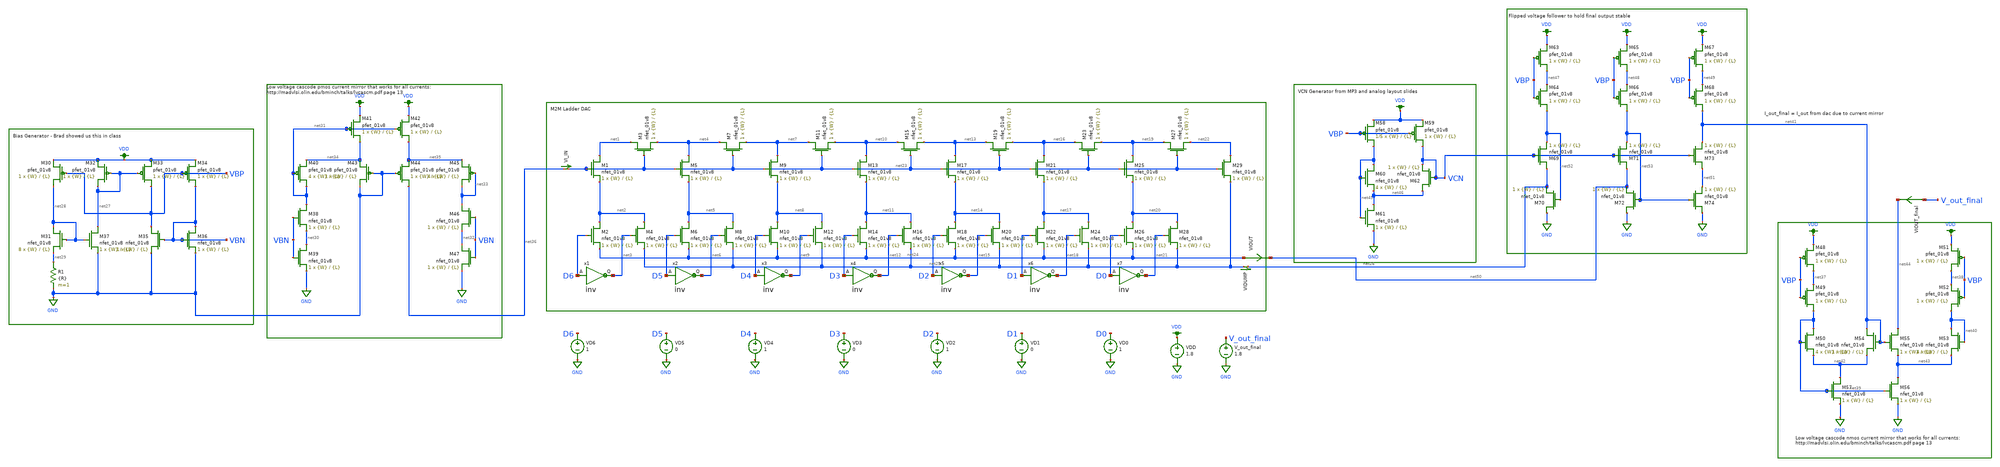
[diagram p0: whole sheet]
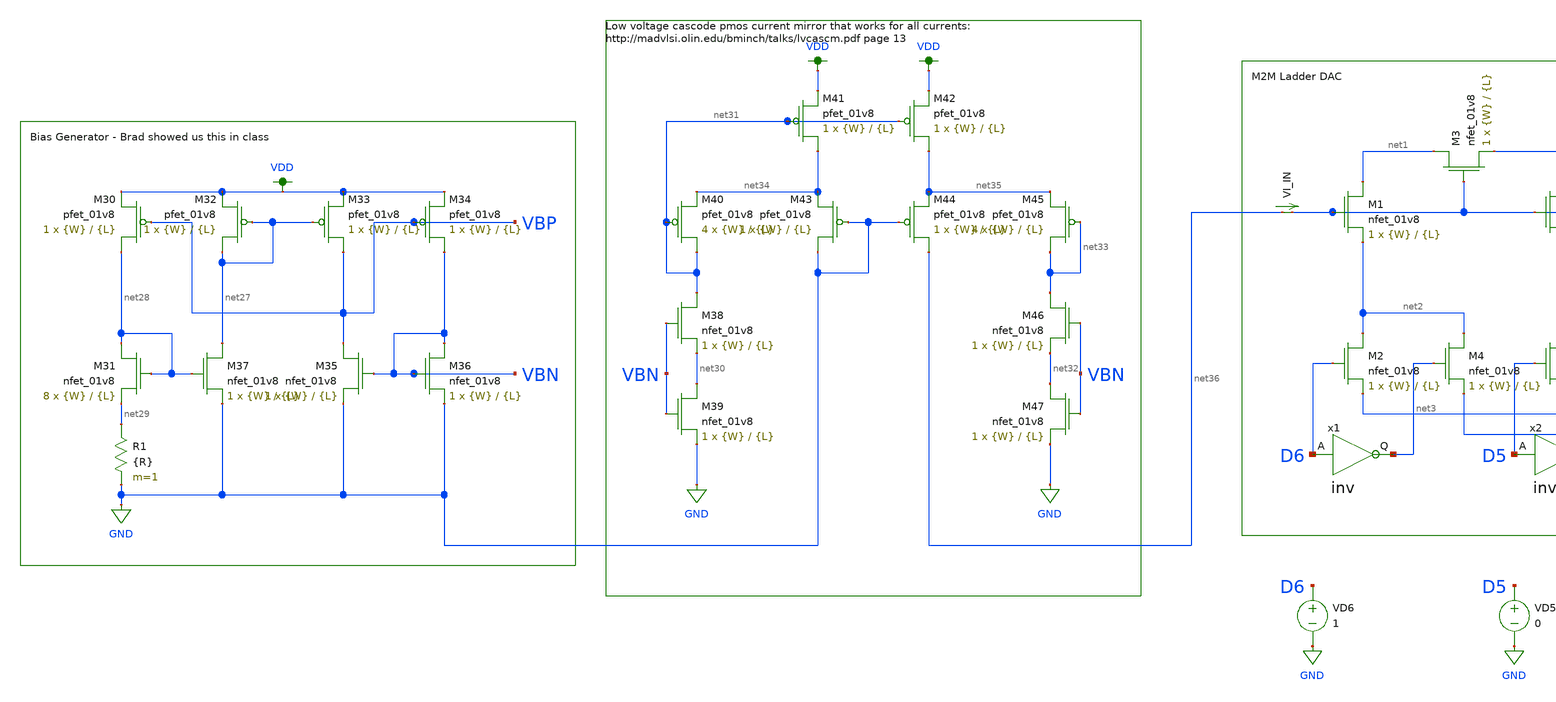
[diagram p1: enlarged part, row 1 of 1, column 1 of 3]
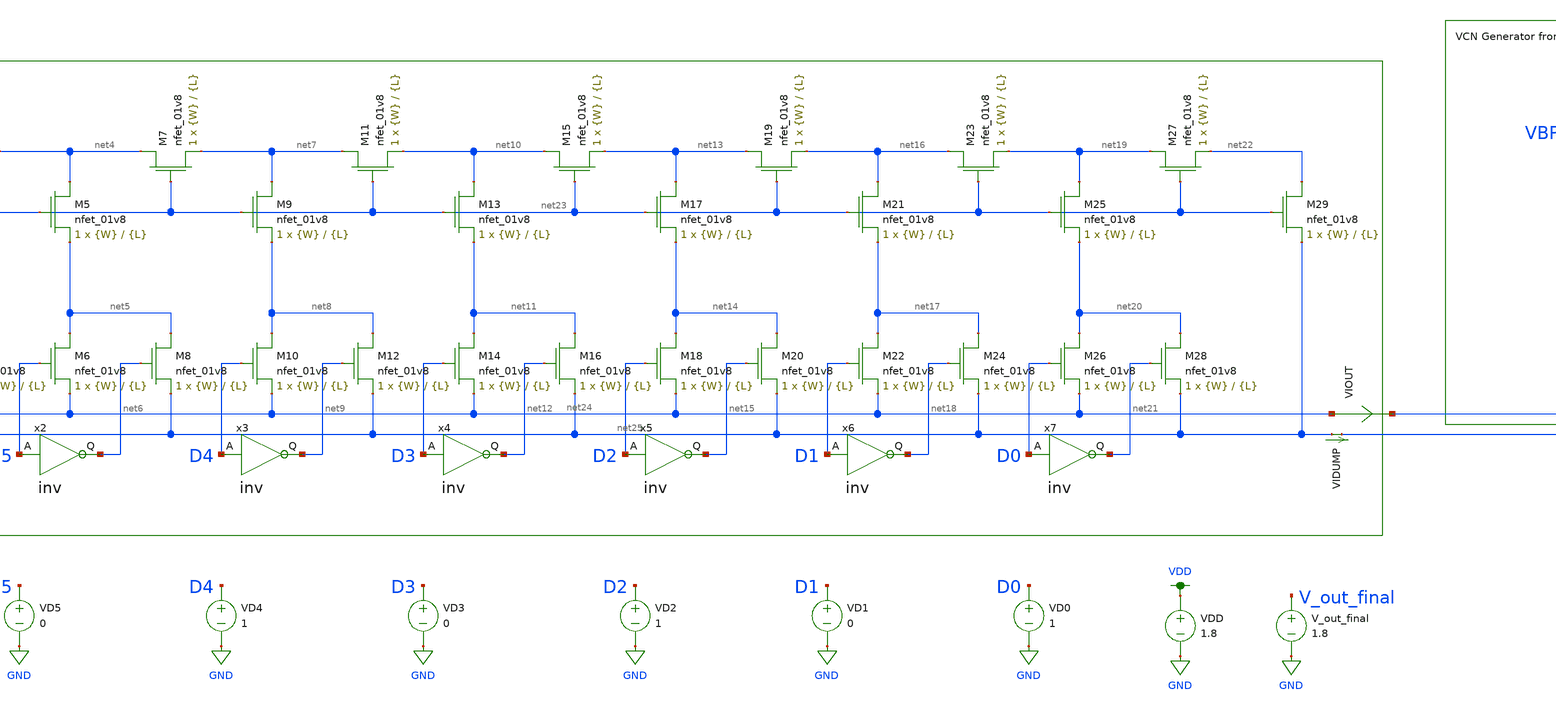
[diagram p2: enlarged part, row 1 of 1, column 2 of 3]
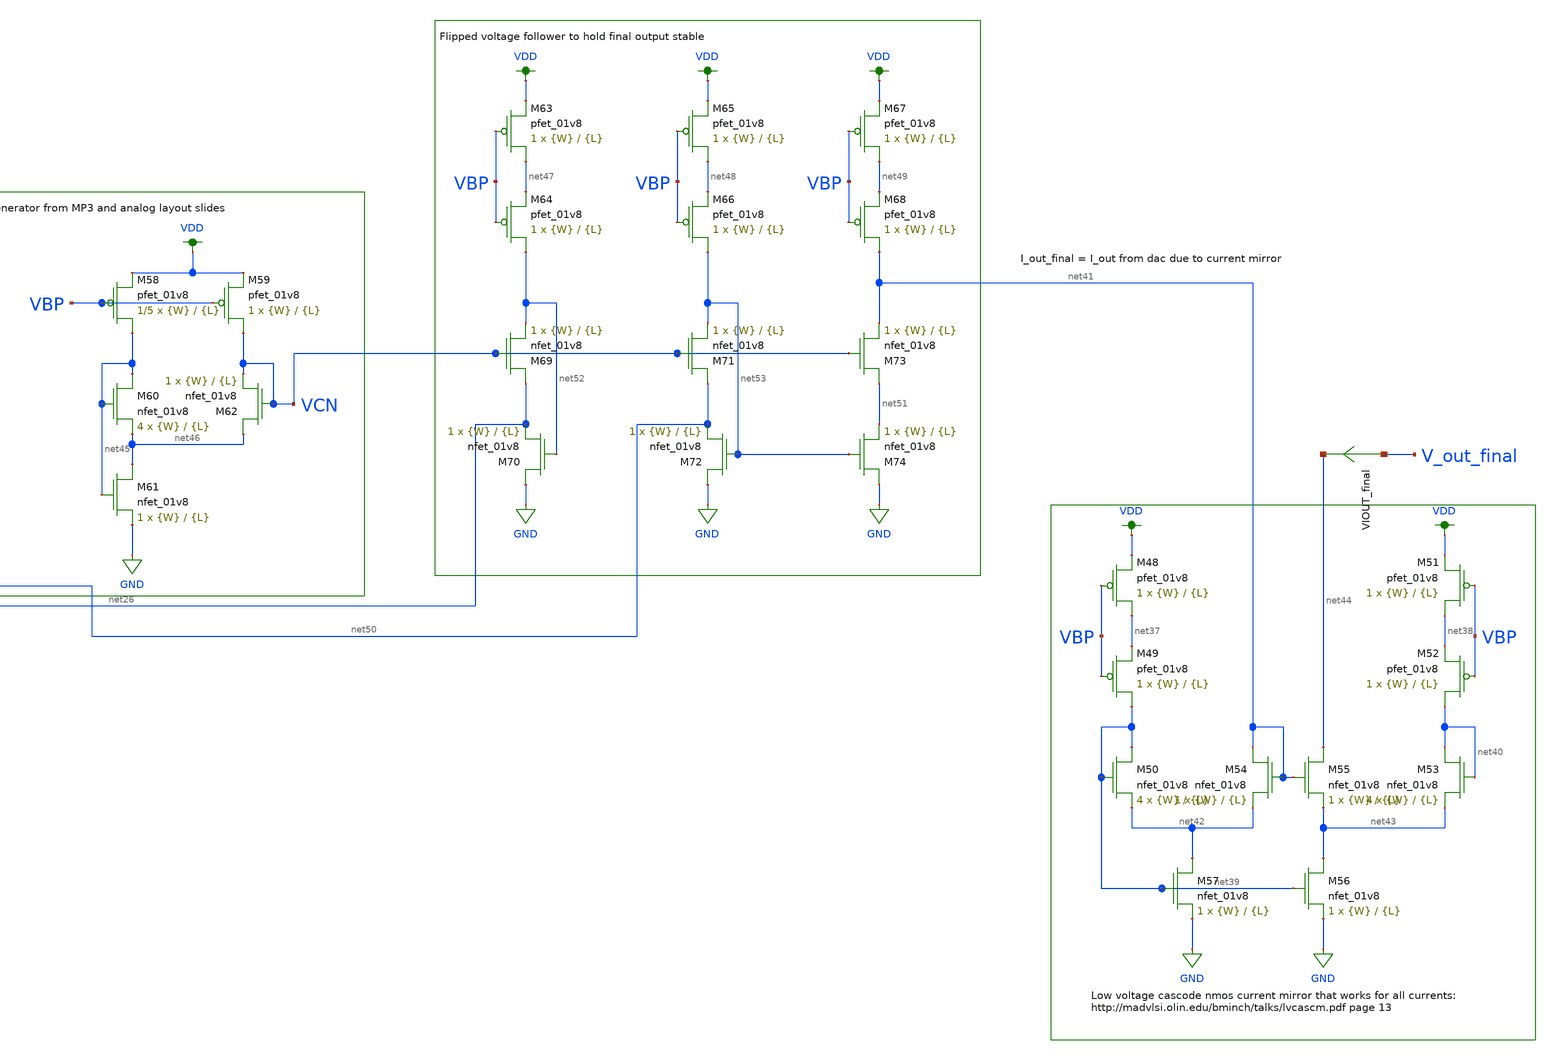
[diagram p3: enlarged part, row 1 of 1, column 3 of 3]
** sch_path: top_dac_VTC.sch
**.subckt top_dac_VTC
XM1 net1 net23 net2 GND sky130_fd_pr__nfet_01v8 L={L} W={W} nf=1 ad='int((nf+1)/2) * W/nf * 0.29' as='int((nf+2)/2) * W/nf * 0.29'
+ pd='2*int((nf+1)/2) * (W/nf + 0.29)' ps='2*int((nf+2)/2) * (W/nf + 0.29)' nrd='0.29 / W' nrs='0.29 / W'
+ sa=0 sb=0 sd=0 mult=1 m=1
XM2 net2 D6 net24 GND sky130_fd_pr__nfet_01v8 L={L} W={W} nf=1 ad='int((nf+1)/2) * W/nf * 0.29' as='int((nf+2)/2) * W/nf * 0.29'
+ pd='2*int((nf+1)/2) * (W/nf + 0.29)' ps='2*int((nf+2)/2) * (W/nf + 0.29)' nrd='0.29 / W' nrs='0.29 / W'
+ sa=0 sb=0 sd=0 mult=1 m=1
XM3 net1 net23 net4 GND sky130_fd_pr__nfet_01v8 L={L} W={W} nf=1 ad='int((nf+1)/2) * W/nf * 0.29' as='int((nf+2)/2) * W/nf * 0.29'
+ pd='2*int((nf+1)/2) * (W/nf + 0.29)' ps='2*int((nf+2)/2) * (W/nf + 0.29)' nrd='0.29 / W' nrs='0.29 / W'
+ sa=0 sb=0 sd=0 mult=1 m=1
XM4 net2 net3 net25 GND sky130_fd_pr__nfet_01v8 L={L} W={W} nf=1 ad='int((nf+1)/2) * W/nf * 0.29' as='int((nf+2)/2) * W/nf * 0.29'
+ pd='2*int((nf+1)/2) * (W/nf + 0.29)' ps='2*int((nf+2)/2) * (W/nf + 0.29)' nrd='0.29 / W' nrs='0.29 / W'
+ sa=0 sb=0 sd=0 mult=1 m=1
XM5 net4 net23 net5 GND sky130_fd_pr__nfet_01v8 L={L} W={W} nf=1 ad='int((nf+1)/2) * W/nf * 0.29' as='int((nf+2)/2) * W/nf * 0.29'
+ pd='2*int((nf+1)/2) * (W/nf + 0.29)' ps='2*int((nf+2)/2) * (W/nf + 0.29)' nrd='0.29 / W' nrs='0.29 / W'
+ sa=0 sb=0 sd=0 mult=1 m=1
XM6 net5 D5 net24 GND sky130_fd_pr__nfet_01v8 L={L} W={W} nf=1 ad='int((nf+1)/2) * W/nf * 0.29' as='int((nf+2)/2) * W/nf * 0.29'
+ pd='2*int((nf+1)/2) * (W/nf + 0.29)' ps='2*int((nf+2)/2) * (W/nf + 0.29)' nrd='0.29 / W' nrs='0.29 / W'
+ sa=0 sb=0 sd=0 mult=1 m=1
XM7 net4 net23 net7 GND sky130_fd_pr__nfet_01v8 L={L} W={W} nf=1 ad='int((nf+1)/2) * W/nf * 0.29' as='int((nf+2)/2) * W/nf * 0.29'
+ pd='2*int((nf+1)/2) * (W/nf + 0.29)' ps='2*int((nf+2)/2) * (W/nf + 0.29)' nrd='0.29 / W' nrs='0.29 / W'
+ sa=0 sb=0 sd=0 mult=1 m=1
XM8 net5 net6 net25 GND sky130_fd_pr__nfet_01v8 L={L} W={W} nf=1 ad='int((nf+1)/2) * W/nf * 0.29' as='int((nf+2)/2) * W/nf * 0.29'
+ pd='2*int((nf+1)/2) * (W/nf + 0.29)' ps='2*int((nf+2)/2) * (W/nf + 0.29)' nrd='0.29 / W' nrs='0.29 / W'
+ sa=0 sb=0 sd=0 mult=1 m=1
XM9 net7 net23 net8 GND sky130_fd_pr__nfet_01v8 L={L} W={W} nf=1 ad='int((nf+1)/2) * W/nf * 0.29' as='int((nf+2)/2) * W/nf * 0.29'
+ pd='2*int((nf+1)/2) * (W/nf + 0.29)' ps='2*int((nf+2)/2) * (W/nf + 0.29)' nrd='0.29 / W' nrs='0.29 / W'
+ sa=0 sb=0 sd=0 mult=1 m=1
XM10 net8 D4 net24 GND sky130_fd_pr__nfet_01v8 L={L} W={W} nf=1 ad='int((nf+1)/2) * W/nf * 0.29' as='int((nf+2)/2) * W/nf * 0.29'
+ pd='2*int((nf+1)/2) * (W/nf + 0.29)' ps='2*int((nf+2)/2) * (W/nf + 0.29)' nrd='0.29 / W' nrs='0.29 / W'
+ sa=0 sb=0 sd=0 mult=1 m=1
XM11 net7 net23 net10 GND sky130_fd_pr__nfet_01v8 L={L} W={W} nf=1 ad='int((nf+1)/2) * W/nf * 0.29' as='int((nf+2)/2) * W/nf * 0.29'
+ pd='2*int((nf+1)/2) * (W/nf + 0.29)' ps='2*int((nf+2)/2) * (W/nf + 0.29)' nrd='0.29 / W' nrs='0.29 / W'
+ sa=0 sb=0 sd=0 mult=1 m=1
XM12 net8 net9 net25 GND sky130_fd_pr__nfet_01v8 L={L} W={W} nf=1 ad='int((nf+1)/2) * W/nf * 0.29' as='int((nf+2)/2) * W/nf * 0.29'
+ pd='2*int((nf+1)/2) * (W/nf + 0.29)' ps='2*int((nf+2)/2) * (W/nf + 0.29)' nrd='0.29 / W' nrs='0.29 / W'
+ sa=0 sb=0 sd=0 mult=1 m=1
XM13 net10 net23 net11 GND sky130_fd_pr__nfet_01v8 L={L} W={W} nf=1 ad='int((nf+1)/2) * W/nf * 0.29'
+ as='int((nf+2)/2) * W/nf * 0.29' pd='2*int((nf+1)/2) * (W/nf + 0.29)' ps='2*int((nf+2)/2) * (W/nf + 0.29)'
+ nrd='0.29 / W' nrs='0.29 / W' sa=0 sb=0 sd=0 mult=1 m=1
XM14 net11 D3 net24 GND sky130_fd_pr__nfet_01v8 L={L} W={W} nf=1 ad='int((nf+1)/2) * W/nf * 0.29' as='int((nf+2)/2) * W/nf * 0.29'
+ pd='2*int((nf+1)/2) * (W/nf + 0.29)' ps='2*int((nf+2)/2) * (W/nf + 0.29)' nrd='0.29 / W' nrs='0.29 / W'
+ sa=0 sb=0 sd=0 mult=1 m=1
XM15 net10 net23 net13 GND sky130_fd_pr__nfet_01v8 L={L} W={W} nf=1 ad='int((nf+1)/2) * W/nf * 0.29'
+ as='int((nf+2)/2) * W/nf * 0.29' pd='2*int((nf+1)/2) * (W/nf + 0.29)' ps='2*int((nf+2)/2) * (W/nf + 0.29)'
+ nrd='0.29 / W' nrs='0.29 / W' sa=0 sb=0 sd=0 mult=1 m=1
XM16 net11 net12 net25 GND sky130_fd_pr__nfet_01v8 L={L} W={W} nf=1 ad='int((nf+1)/2) * W/nf * 0.29'
+ as='int((nf+2)/2) * W/nf * 0.29' pd='2*int((nf+1)/2) * (W/nf + 0.29)' ps='2*int((nf+2)/2) * (W/nf + 0.29)'
+ nrd='0.29 / W' nrs='0.29 / W' sa=0 sb=0 sd=0 mult=1 m=1
XM17 net13 net23 net14 GND sky130_fd_pr__nfet_01v8 L={L} W={W} nf=1 ad='int((nf+1)/2) * W/nf * 0.29'
+ as='int((nf+2)/2) * W/nf * 0.29' pd='2*int((nf+1)/2) * (W/nf + 0.29)' ps='2*int((nf+2)/2) * (W/nf + 0.29)'
+ nrd='0.29 / W' nrs='0.29 / W' sa=0 sb=0 sd=0 mult=1 m=1
XM18 net14 D2 net24 GND sky130_fd_pr__nfet_01v8 L={L} W={W} nf=1 ad='int((nf+1)/2) * W/nf * 0.29' as='int((nf+2)/2) * W/nf * 0.29'
+ pd='2*int((nf+1)/2) * (W/nf + 0.29)' ps='2*int((nf+2)/2) * (W/nf + 0.29)' nrd='0.29 / W' nrs='0.29 / W'
+ sa=0 sb=0 sd=0 mult=1 m=1
XM19 net13 net23 net16 GND sky130_fd_pr__nfet_01v8 L={L} W={W} nf=1 ad='int((nf+1)/2) * W/nf * 0.29'
+ as='int((nf+2)/2) * W/nf * 0.29' pd='2*int((nf+1)/2) * (W/nf + 0.29)' ps='2*int((nf+2)/2) * (W/nf + 0.29)'
+ nrd='0.29 / W' nrs='0.29 / W' sa=0 sb=0 sd=0 mult=1 m=1
XM20 net14 net15 net25 GND sky130_fd_pr__nfet_01v8 L={L} W={W} nf=1 ad='int((nf+1)/2) * W/nf * 0.29'
+ as='int((nf+2)/2) * W/nf * 0.29' pd='2*int((nf+1)/2) * (W/nf + 0.29)' ps='2*int((nf+2)/2) * (W/nf + 0.29)'
+ nrd='0.29 / W' nrs='0.29 / W' sa=0 sb=0 sd=0 mult=1 m=1
XM21 net16 net23 net17 GND sky130_fd_pr__nfet_01v8 L={L} W={W} nf=1 ad='int((nf+1)/2) * W/nf * 0.29'
+ as='int((nf+2)/2) * W/nf * 0.29' pd='2*int((nf+1)/2) * (W/nf + 0.29)' ps='2*int((nf+2)/2) * (W/nf + 0.29)'
+ nrd='0.29 / W' nrs='0.29 / W' sa=0 sb=0 sd=0 mult=1 m=1
XM22 net17 D1 net24 GND sky130_fd_pr__nfet_01v8 L={L} W={W} nf=1 ad='int((nf+1)/2) * W/nf * 0.29' as='int((nf+2)/2) * W/nf * 0.29'
+ pd='2*int((nf+1)/2) * (W/nf + 0.29)' ps='2*int((nf+2)/2) * (W/nf + 0.29)' nrd='0.29 / W' nrs='0.29 / W'
+ sa=0 sb=0 sd=0 mult=1 m=1
XM23 net16 net23 net19 GND sky130_fd_pr__nfet_01v8 L={L} W={W} nf=1 ad='int((nf+1)/2) * W/nf * 0.29'
+ as='int((nf+2)/2) * W/nf * 0.29' pd='2*int((nf+1)/2) * (W/nf + 0.29)' ps='2*int((nf+2)/2) * (W/nf + 0.29)'
+ nrd='0.29 / W' nrs='0.29 / W' sa=0 sb=0 sd=0 mult=1 m=1
XM24 net17 net18 net25 GND sky130_fd_pr__nfet_01v8 L={L} W={W} nf=1 ad='int((nf+1)/2) * W/nf * 0.29'
+ as='int((nf+2)/2) * W/nf * 0.29' pd='2*int((nf+1)/2) * (W/nf + 0.29)' ps='2*int((nf+2)/2) * (W/nf + 0.29)'
+ nrd='0.29 / W' nrs='0.29 / W' sa=0 sb=0 sd=0 mult=1 m=1
XM25 net19 net23 net20 GND sky130_fd_pr__nfet_01v8 L={L} W={W} nf=1 ad='int((nf+1)/2) * W/nf * 0.29'
+ as='int((nf+2)/2) * W/nf * 0.29' pd='2*int((nf+1)/2) * (W/nf + 0.29)' ps='2*int((nf+2)/2) * (W/nf + 0.29)'
+ nrd='0.29 / W' nrs='0.29 / W' sa=0 sb=0 sd=0 mult=1 m=1
XM26 net20 D0 net24 GND sky130_fd_pr__nfet_01v8 L={L} W={W} nf=1 ad='int((nf+1)/2) * W/nf * 0.29' as='int((nf+2)/2) * W/nf * 0.29'
+ pd='2*int((nf+1)/2) * (W/nf + 0.29)' ps='2*int((nf+2)/2) * (W/nf + 0.29)' nrd='0.29 / W' nrs='0.29 / W'
+ sa=0 sb=0 sd=0 mult=1 m=1
XM27 net19 net23 net22 GND sky130_fd_pr__nfet_01v8 L={L} W={W} nf=1 ad='int((nf+1)/2) * W/nf * 0.29'
+ as='int((nf+2)/2) * W/nf * 0.29' pd='2*int((nf+1)/2) * (W/nf + 0.29)' ps='2*int((nf+2)/2) * (W/nf + 0.29)'
+ nrd='0.29 / W' nrs='0.29 / W' sa=0 sb=0 sd=0 mult=1 m=1
XM28 net20 net21 net25 GND sky130_fd_pr__nfet_01v8 L={L} W={W} nf=1 ad='int((nf+1)/2) * W/nf * 0.29'
+ as='int((nf+2)/2) * W/nf * 0.29' pd='2*int((nf+1)/2) * (W/nf + 0.29)' ps='2*int((nf+2)/2) * (W/nf + 0.29)'
+ nrd='0.29 / W' nrs='0.29 / W' sa=0 sb=0 sd=0 mult=1 m=1
XM29 net22 net23 net25 GND sky130_fd_pr__nfet_01v8 L={L} W={W} nf=1 ad='int((nf+1)/2) * W/nf * 0.29'
+ as='int((nf+2)/2) * W/nf * 0.29' pd='2*int((nf+1)/2) * (W/nf + 0.29)' ps='2*int((nf+2)/2) * (W/nf + 0.29)'
+ nrd='0.29 / W' nrs='0.29 / W' sa=0 sb=0 sd=0 mult=1 m=1
VIDUMP net25 net26 0
.save i(vidump)
VI_IN net36 net23 0
.save i(vi_in)
x1 net3 D6 inv
x2 net6 D5 inv
x3 net9 D4 inv
x4 net12 D3 inv
x5 net15 D2 inv
x6 net18 D1 inv
x7 net21 D0 inv
XM30 net28 VBP VDD VDD sky130_fd_pr__pfet_01v8 L={L} W={W} nf=1 ad='int((nf+1)/2) * W/nf * 0.29' as='int((nf+2)/2) * W/nf * 0.29'
+ pd='2*int((nf+1)/2) * (W/nf + 0.29)' ps='2*int((nf+2)/2) * (W/nf + 0.29)' nrd='0.29 / W' nrs='0.29 / W'
+ sa=0 sb=0 sd=0 mult=1 m=1
XM31 net28 net28 net29 GND sky130_fd_pr__nfet_01v8 L={L} W={W} nf=1 ad='int((nf+1)/2) * W/nf * 0.29'
+ as='int((nf+2)/2) * W/nf * 0.29' pd='2*int((nf+1)/2) * (W/nf + 0.29)' ps='2*int((nf+2)/2) * (W/nf + 0.29)'
+ nrd='0.29 / W' nrs='0.29 / W' sa=0 sb=0 sd=0 mult=8 m=8
XM32 net27 net27 VDD VDD sky130_fd_pr__pfet_01v8 L={L} W={W} nf=1 ad='int((nf+1)/2) * W/nf * 0.29' as='int((nf+2)/2) * W/nf * 0.29'
+ pd='2*int((nf+1)/2) * (W/nf + 0.29)' ps='2*int((nf+2)/2) * (W/nf + 0.29)' nrd='0.29 / W' nrs='0.29 / W'
+ sa=0 sb=0 sd=0 mult=1 m=1
XM33 VBP net27 VDD VDD sky130_fd_pr__pfet_01v8 L={L} W={W} nf=1 ad='int((nf+1)/2) * W/nf * 0.29' as='int((nf+2)/2) * W/nf * 0.29'
+ pd='2*int((nf+1)/2) * (W/nf + 0.29)' ps='2*int((nf+2)/2) * (W/nf + 0.29)' nrd='0.29 / W' nrs='0.29 / W'
+ sa=0 sb=0 sd=0 mult=1 m=1
XM34 VBN VBP VDD VDD sky130_fd_pr__pfet_01v8 L={L} W={W} nf=1 ad='int((nf+1)/2) * W/nf * 0.29' as='int((nf+2)/2) * W/nf * 0.29'
+ pd='2*int((nf+1)/2) * (W/nf + 0.29)' ps='2*int((nf+2)/2) * (W/nf + 0.29)' nrd='0.29 / W' nrs='0.29 / W'
+ sa=0 sb=0 sd=0 mult=1 m=1
XM35 VBP VBN GND GND sky130_fd_pr__nfet_01v8 L={L} W={W} nf=1 ad='int((nf+1)/2) * W/nf * 0.29' as='int((nf+2)/2) * W/nf * 0.29'
+ pd='2*int((nf+1)/2) * (W/nf + 0.29)' ps='2*int((nf+2)/2) * (W/nf + 0.29)' nrd='0.29 / W' nrs='0.29 / W'
+ sa=0 sb=0 sd=0 mult=1 m=1
XM36 VBN VBN GND GND sky130_fd_pr__nfet_01v8 L={L} W={W} nf=1 ad='int((nf+1)/2) * W/nf * 0.29' as='int((nf+2)/2) * W/nf * 0.29'
+ pd='2*int((nf+1)/2) * (W/nf + 0.29)' ps='2*int((nf+2)/2) * (W/nf + 0.29)' nrd='0.29 / W' nrs='0.29 / W'
+ sa=0 sb=0 sd=0 mult=1 m=1
XM37 net27 net28 GND GND sky130_fd_pr__nfet_01v8 L={L} W={W} nf=1 ad='int((nf+1)/2) * W/nf * 0.29' as='int((nf+2)/2) * W/nf * 0.29'
+ pd='2*int((nf+1)/2) * (W/nf + 0.29)' ps='2*int((nf+2)/2) * (W/nf + 0.29)' nrd='0.29 / W' nrs='0.29 / W'
+ sa=0 sb=0 sd=0 mult=1 m=1
R1 net29 GND {R} m=1
XM38 net31 VBN net30 GND sky130_fd_pr__nfet_01v8 L={L} W={W} nf=1 ad='int((nf+1)/2) * W/nf * 0.29' as='int((nf+2)/2) * W/nf * 0.29'
+ pd='2*int((nf+1)/2) * (W/nf + 0.29)' ps='2*int((nf+2)/2) * (W/nf + 0.29)' nrd='0.29 / W' nrs='0.29 / W'
+ sa=0 sb=0 sd=0 mult=1 m=1
XM39 net30 VBN GND GND sky130_fd_pr__nfet_01v8 L={L} W={W} nf=1 ad='int((nf+1)/2) * W/nf * 0.29' as='int((nf+2)/2) * W/nf * 0.29'
+ pd='2*int((nf+1)/2) * (W/nf + 0.29)' ps='2*int((nf+2)/2) * (W/nf + 0.29)' nrd='0.29 / W' nrs='0.29 / W'
+ sa=0 sb=0 sd=0 mult=1 m=1
XM40 net31 net31 net34 VDD sky130_fd_pr__pfet_01v8 L={L} W={W} nf=1 ad='int((nf+1)/2) * W/nf * 0.29'
+ as='int((nf+2)/2) * W/nf * 0.29' pd='2*int((nf+1)/2) * (W/nf + 0.29)' ps='2*int((nf+2)/2) * (W/nf + 0.29)'
+ nrd='0.29 / W' nrs='0.29 / W' sa=0 sb=0 sd=0 mult=4 m=4
XM41 net34 net31 VDD VDD sky130_fd_pr__pfet_01v8 L={L} W={W} nf=1 ad='int((nf+1)/2) * W/nf * 0.29' as='int((nf+2)/2) * W/nf * 0.29'
+ pd='2*int((nf+1)/2) * (W/nf + 0.29)' ps='2*int((nf+2)/2) * (W/nf + 0.29)' nrd='0.29 / W' nrs='0.29 / W'
+ sa=0 sb=0 sd=0 mult=1 m=1
XM42 net35 net31 VDD VDD sky130_fd_pr__pfet_01v8 L={L} W={W} nf=1 ad='int((nf+1)/2) * W/nf * 0.29' as='int((nf+2)/2) * W/nf * 0.29'
+ pd='2*int((nf+1)/2) * (W/nf + 0.29)' ps='2*int((nf+2)/2) * (W/nf + 0.29)' nrd='0.29 / W' nrs='0.29 / W'
+ sa=0 sb=0 sd=0 mult=1 m=1
XM43 GND GND net34 VDD sky130_fd_pr__pfet_01v8 L={L} W={W} nf=1 ad='int((nf+1)/2) * W/nf * 0.29' as='int((nf+2)/2) * W/nf * 0.29'
+ pd='2*int((nf+1)/2) * (W/nf + 0.29)' ps='2*int((nf+2)/2) * (W/nf + 0.29)' nrd='0.29 / W' nrs='0.29 / W'
+ sa=0 sb=0 sd=0 mult=1 m=1
XM44 net36 GND net35 VDD sky130_fd_pr__pfet_01v8 L={L} W={W} nf=1 ad='int((nf+1)/2) * W/nf * 0.29' as='int((nf+2)/2) * W/nf * 0.29'
+ pd='2*int((nf+1)/2) * (W/nf + 0.29)' ps='2*int((nf+2)/2) * (W/nf + 0.29)' nrd='0.29 / W' nrs='0.29 / W'
+ sa=0 sb=0 sd=0 mult=1 m=1
XM45 net33 net33 net35 VDD sky130_fd_pr__pfet_01v8 L={L} W={W} nf=1 ad='int((nf+1)/2) * W/nf * 0.29'
+ as='int((nf+2)/2) * W/nf * 0.29' pd='2*int((nf+1)/2) * (W/nf + 0.29)' ps='2*int((nf+2)/2) * (W/nf + 0.29)'
+ nrd='0.29 / W' nrs='0.29 / W' sa=0 sb=0 sd=0 mult=4 m=4
XM46 net33 VBN net32 GND sky130_fd_pr__nfet_01v8 L={L} W={W} nf=1 ad='int((nf+1)/2) * W/nf * 0.29' as='int((nf+2)/2) * W/nf * 0.29'
+ pd='2*int((nf+1)/2) * (W/nf + 0.29)' ps='2*int((nf+2)/2) * (W/nf + 0.29)' nrd='0.29 / W' nrs='0.29 / W'
+ sa=0 sb=0 sd=0 mult=1 m=1
XM47 net32 VBN GND GND sky130_fd_pr__nfet_01v8 L={L} W={W} nf=1 ad='int((nf+1)/2) * W/nf * 0.29' as='int((nf+2)/2) * W/nf * 0.29'
+ pd='2*int((nf+1)/2) * (W/nf + 0.29)' ps='2*int((nf+2)/2) * (W/nf + 0.29)' nrd='0.29 / W' nrs='0.29 / W'
+ sa=0 sb=0 sd=0 mult=1 m=1
XM48 net37 VBP VDD VDD sky130_fd_pr__pfet_01v8 L={L} W={W} nf=1 ad='int((nf+1)/2) * W/nf * 0.29' as='int((nf+2)/2) * W/nf * 0.29'
+ pd='2*int((nf+1)/2) * (W/nf + 0.29)' ps='2*int((nf+2)/2) * (W/nf + 0.29)' nrd='0.29 / W' nrs='0.29 / W'
+ sa=0 sb=0 sd=0 mult=1 m=1
XM49 net39 VBP net37 VDD sky130_fd_pr__pfet_01v8 L={L} W={W} nf=1 ad='int((nf+1)/2) * W/nf * 0.29' as='int((nf+2)/2) * W/nf * 0.29'
+ pd='2*int((nf+1)/2) * (W/nf + 0.29)' ps='2*int((nf+2)/2) * (W/nf + 0.29)' nrd='0.29 / W' nrs='0.29 / W'
+ sa=0 sb=0 sd=0 mult=1 m=1
XM50 net39 net39 net42 GND sky130_fd_pr__nfet_01v8 L={L} W={W} nf=1 ad='int((nf+1)/2) * W/nf * 0.29'
+ as='int((nf+2)/2) * W/nf * 0.29' pd='2*int((nf+1)/2) * (W/nf + 0.29)' ps='2*int((nf+2)/2) * (W/nf + 0.29)'
+ nrd='0.29 / W' nrs='0.29 / W' sa=0 sb=0 sd=0 mult=4 m=4
XM51 net38 VBP VDD VDD sky130_fd_pr__pfet_01v8 L={L} W={W} nf=1 ad='int((nf+1)/2) * W/nf * 0.29' as='int((nf+2)/2) * W/nf * 0.29'
+ pd='2*int((nf+1)/2) * (W/nf + 0.29)' ps='2*int((nf+2)/2) * (W/nf + 0.29)' nrd='0.29 / W' nrs='0.29 / W'
+ sa=0 sb=0 sd=0 mult=1 m=1
XM52 net40 VBP net38 VDD sky130_fd_pr__pfet_01v8 L={L} W={W} nf=1 ad='int((nf+1)/2) * W/nf * 0.29' as='int((nf+2)/2) * W/nf * 0.29'
+ pd='2*int((nf+1)/2) * (W/nf + 0.29)' ps='2*int((nf+2)/2) * (W/nf + 0.29)' nrd='0.29 / W' nrs='0.29 / W'
+ sa=0 sb=0 sd=0 mult=1 m=1
XM53 net40 net40 net43 GND sky130_fd_pr__nfet_01v8 L={L} W={W} nf=1 ad='int((nf+1)/2) * W/nf * 0.29'
+ as='int((nf+2)/2) * W/nf * 0.29' pd='2*int((nf+1)/2) * (W/nf + 0.29)' ps='2*int((nf+2)/2) * (W/nf + 0.29)'
+ nrd='0.29 / W' nrs='0.29 / W' sa=0 sb=0 sd=0 mult=4 m=4
XM54 net41 net41 net42 GND sky130_fd_pr__nfet_01v8 L={L} W={W} nf=1 ad='int((nf+1)/2) * W/nf * 0.29'
+ as='int((nf+2)/2) * W/nf * 0.29' pd='2*int((nf+1)/2) * (W/nf + 0.29)' ps='2*int((nf+2)/2) * (W/nf + 0.29)'
+ nrd='0.29 / W' nrs='0.29 / W' sa=0 sb=0 sd=0 mult=1 m=1
XM55 net44 net41 net43 GND sky130_fd_pr__nfet_01v8 L={L} W={W} nf=1 ad='int((nf+1)/2) * W/nf * 0.29'
+ as='int((nf+2)/2) * W/nf * 0.29' pd='2*int((nf+1)/2) * (W/nf + 0.29)' ps='2*int((nf+2)/2) * (W/nf + 0.29)'
+ nrd='0.29 / W' nrs='0.29 / W' sa=0 sb=0 sd=0 mult=1 m=1
XM56 net43 net39 GND GND sky130_fd_pr__nfet_01v8 L={L} W={W} nf=1 ad='int((nf+1)/2) * W/nf * 0.29' as='int((nf+2)/2) * W/nf * 0.29'
+ pd='2*int((nf+1)/2) * (W/nf + 0.29)' ps='2*int((nf+2)/2) * (W/nf + 0.29)' nrd='0.29 / W' nrs='0.29 / W'
+ sa=0 sb=0 sd=0 mult=1 m=1
XM57 net42 net39 GND GND sky130_fd_pr__nfet_01v8 L={L} W={W} nf=1 ad='int((nf+1)/2) * W/nf * 0.29' as='int((nf+2)/2) * W/nf * 0.29'
+ pd='2*int((nf+1)/2) * (W/nf + 0.29)' ps='2*int((nf+2)/2) * (W/nf + 0.29)' nrd='0.29 / W' nrs='0.29 / W'
+ sa=0 sb=0 sd=0 mult=1 m=1
XM58 net45 VBP VDD VDD sky130_fd_pr__pfet_01v8 L={L} W={W} nf=1 ad='int((nf+1)/2) * W/nf * 0.29' as='int((nf+2)/2) * W/nf * 0.29'
+ pd='2*int((nf+1)/2) * (W/nf + 0.29)' ps='2*int((nf+2)/2) * (W/nf + 0.29)' nrd='0.29 / W' nrs='0.29 / W'
+ sa=0 sb=0 sd=0 mult=1/5 m=1/5
XM59 VCN VBP VDD VDD sky130_fd_pr__pfet_01v8 L={L} W={W} nf=1 ad='int((nf+1)/2) * W/nf * 0.29' as='int((nf+2)/2) * W/nf * 0.29'
+ pd='2*int((nf+1)/2) * (W/nf + 0.29)' ps='2*int((nf+2)/2) * (W/nf + 0.29)' nrd='0.29 / W' nrs='0.29 / W'
+ sa=0 sb=0 sd=0 mult=1 m=1
XM60 net45 net45 net46 GND sky130_fd_pr__nfet_01v8 L={L} W={W} nf=1 ad='int((nf+1)/2) * W/nf * 0.29'
+ as='int((nf+2)/2) * W/nf * 0.29' pd='2*int((nf+1)/2) * (W/nf + 0.29)' ps='2*int((nf+2)/2) * (W/nf + 0.29)'
+ nrd='0.29 / W' nrs='0.29 / W' sa=0 sb=0 sd=0 mult=4 m=4
XM61 net46 net45 GND GND sky130_fd_pr__nfet_01v8 L={L} W={W} nf=1 ad='int((nf+1)/2) * W/nf * 0.29' as='int((nf+2)/2) * W/nf * 0.29'
+ pd='2*int((nf+1)/2) * (W/nf + 0.29)' ps='2*int((nf+2)/2) * (W/nf + 0.29)' nrd='0.29 / W' nrs='0.29 / W'
+ sa=0 sb=0 sd=0 mult=1 m=1
XM62 net46 VCN VCN GND sky130_fd_pr__nfet_01v8 L={L} W={W} nf=1 ad='int((nf+1)/2) * W/nf * 0.29' as='int((nf+2)/2) * W/nf * 0.29'
+ pd='2*int((nf+1)/2) * (W/nf + 0.29)' ps='2*int((nf+2)/2) * (W/nf + 0.29)' nrd='0.29 / W' nrs='0.29 / W'
+ sa=0 sb=0 sd=0 mult=1 m=1
XM63 net47 VBP VDD VDD sky130_fd_pr__pfet_01v8 L={L} W={W} nf=1 ad='int((nf+1)/2) * W/nf * 0.29' as='int((nf+2)/2) * W/nf * 0.29'
+ pd='2*int((nf+1)/2) * (W/nf + 0.29)' ps='2*int((nf+2)/2) * (W/nf + 0.29)' nrd='0.29 / W' nrs='0.29 / W'
+ sa=0 sb=0 sd=0 mult=1 m=1
XM64 net52 VBP net47 VDD sky130_fd_pr__pfet_01v8 L={L} W={W} nf=1 ad='int((nf+1)/2) * W/nf * 0.29' as='int((nf+2)/2) * W/nf * 0.29'
+ pd='2*int((nf+1)/2) * (W/nf + 0.29)' ps='2*int((nf+2)/2) * (W/nf + 0.29)' nrd='0.29 / W' nrs='0.29 / W'
+ sa=0 sb=0 sd=0 mult=1 m=1
XM65 net48 VBP VDD VDD sky130_fd_pr__pfet_01v8 L={L} W={W} nf=1 ad='int((nf+1)/2) * W/nf * 0.29' as='int((nf+2)/2) * W/nf * 0.29'
+ pd='2*int((nf+1)/2) * (W/nf + 0.29)' ps='2*int((nf+2)/2) * (W/nf + 0.29)' nrd='0.29 / W' nrs='0.29 / W'
+ sa=0 sb=0 sd=0 mult=1 m=1
XM66 net53 VBP net48 VDD sky130_fd_pr__pfet_01v8 L={L} W={W} nf=1 ad='int((nf+1)/2) * W/nf * 0.29' as='int((nf+2)/2) * W/nf * 0.29'
+ pd='2*int((nf+1)/2) * (W/nf + 0.29)' ps='2*int((nf+2)/2) * (W/nf + 0.29)' nrd='0.29 / W' nrs='0.29 / W'
+ sa=0 sb=0 sd=0 mult=1 m=1
XM67 net49 VBP VDD VDD sky130_fd_pr__pfet_01v8 L={L} W={W} nf=1 ad='int((nf+1)/2) * W/nf * 0.29' as='int((nf+2)/2) * W/nf * 0.29'
+ pd='2*int((nf+1)/2) * (W/nf + 0.29)' ps='2*int((nf+2)/2) * (W/nf + 0.29)' nrd='0.29 / W' nrs='0.29 / W'
+ sa=0 sb=0 sd=0 mult=1 m=1
XM68 net41 VBP net49 VDD sky130_fd_pr__pfet_01v8 L={L} W={W} nf=1 ad='int((nf+1)/2) * W/nf * 0.29' as='int((nf+2)/2) * W/nf * 0.29'
+ pd='2*int((nf+1)/2) * (W/nf + 0.29)' ps='2*int((nf+2)/2) * (W/nf + 0.29)' nrd='0.29 / W' nrs='0.29 / W'
+ sa=0 sb=0 sd=0 mult=1 m=1
XM69 net26 VCN net52 GND sky130_fd_pr__nfet_01v8 L={L} W={W} nf=1 ad='int((nf+1)/2) * W/nf * 0.29' as='int((nf+2)/2) * W/nf * 0.29'
+ pd='2*int((nf+1)/2) * (W/nf + 0.29)' ps='2*int((nf+2)/2) * (W/nf + 0.29)' nrd='0.29 / W' nrs='0.29 / W'
+ sa=0 sb=0 sd=0 mult=1 m=1
XM70 GND net52 net26 GND sky130_fd_pr__nfet_01v8 L={L} W={W} nf=1 ad='int((nf+1)/2) * W/nf * 0.29' as='int((nf+2)/2) * W/nf * 0.29'
+ pd='2*int((nf+1)/2) * (W/nf + 0.29)' ps='2*int((nf+2)/2) * (W/nf + 0.29)' nrd='0.29 / W' nrs='0.29 / W'
+ sa=0 sb=0 sd=0 mult=1 m=1
XM71 net50 VCN net53 GND sky130_fd_pr__nfet_01v8 L={L} W={W} nf=1 ad='int((nf+1)/2) * W/nf * 0.29' as='int((nf+2)/2) * W/nf * 0.29'
+ pd='2*int((nf+1)/2) * (W/nf + 0.29)' ps='2*int((nf+2)/2) * (W/nf + 0.29)' nrd='0.29 / W' nrs='0.29 / W'
+ sa=0 sb=0 sd=0 mult=1 m=1
XM72 GND net53 net50 GND sky130_fd_pr__nfet_01v8 L={L} W={W} nf=1 ad='int((nf+1)/2) * W/nf * 0.29' as='int((nf+2)/2) * W/nf * 0.29'
+ pd='2*int((nf+1)/2) * (W/nf + 0.29)' ps='2*int((nf+2)/2) * (W/nf + 0.29)' nrd='0.29 / W' nrs='0.29 / W'
+ sa=0 sb=0 sd=0 mult=1 m=1
XM73 net51 VCN net41 GND sky130_fd_pr__nfet_01v8 L={L} W={W} nf=1 ad='int((nf+1)/2) * W/nf * 0.29' as='int((nf+2)/2) * W/nf * 0.29'
+ pd='2*int((nf+1)/2) * (W/nf + 0.29)' ps='2*int((nf+2)/2) * (W/nf + 0.29)' nrd='0.29 / W' nrs='0.29 / W'
+ sa=0 sb=0 sd=0 mult=1 m=1
XM74 GND net53 net51 GND sky130_fd_pr__nfet_01v8 L={L} W={W} nf=1 ad='int((nf+1)/2) * W/nf * 0.29' as='int((nf+2)/2) * W/nf * 0.29'
+ pd='2*int((nf+1)/2) * (W/nf + 0.29)' ps='2*int((nf+2)/2) * (W/nf + 0.29)' nrd='0.29 / W' nrs='0.29 / W'
+ sa=0 sb=0 sd=0 mult=1 m=1
VDD VDD GND 1.8
VD6 D6 GND 1
VD1 D1 GND 0
VD2 D2 GND 1
VD3 D3 GND 0
VD4 D4 GND 1
VD5 D5 GND 0
VD0 D0 GND 1
VIOUT net24 net50 0
.save i(viout)
VIOUT_final V_out_final net44 0
.save i(viout_final)
V_out_final V_out_final GND 1.8
**** begin user architecture code

.option wnflag=1
.param MC_SWITCH=0.0
.lib ~/skywater/skywater-pdk/libraries/sky130_fd_pr_ngspice/latest/models/sky130.lib.spice tt


.param W=32 L=4 R=200K
.dc V_out_final 0 1.8 .01
.save v(V_out_final) i(VIOUT_final) i(VI_IN)
.control
set filetype=ascii
run
plot i(VIOUT_final)
write PS_SWEEP.csv i(VIOUT_final)
.endc

**** end user architecture code
**.ends

* expanding   symbol:  /home/mstopyra/Documents/MADVLSI-MP4-DAC/schemas/inv.sym # of pins=2
** sym_path: /home/mstopyra/Documents/MADVLSI-MP4-DAC/schemas/inv.sym
** sch_path: /home/mstopyra/Documents/MADVLSI-MP4-DAC/schemas/inv.sch
.subckt inv Q A
*.ipin A
*.opin Q
XM1 Q A GND GND sky130_fd_pr__nfet_01v8 L=4 W=32 nf=1 ad='int((nf+1)/2) * W/nf * 0.29' as='int((nf+2)/2) * W/nf * 0.29'
+ pd='2*int((nf+1)/2) * (W/nf + 0.29)' ps='2*int((nf+2)/2) * (W/nf + 0.29)' nrd='0.29 / W' nrs='0.29 / W'
+ sa=0 sb=0 sd=0 mult=2 m=2
XM2 Q A VDD VDD sky130_fd_pr__pfet_01v8 L=4 W=32 nf=1 ad='int((nf+1)/2) * W/nf * 0.29' as='int((nf+2)/2) * W/nf * 0.29'
+ pd='2*int((nf+1)/2) * (W/nf + 0.29)' ps='2*int((nf+2)/2) * (W/nf + 0.29)' nrd='0.29 / W' nrs='0.29 / W'
+ sa=0 sb=0 sd=0 mult=1 m=1
.ends

.GLOBAL GND
.GLOBAL VDD
.end
